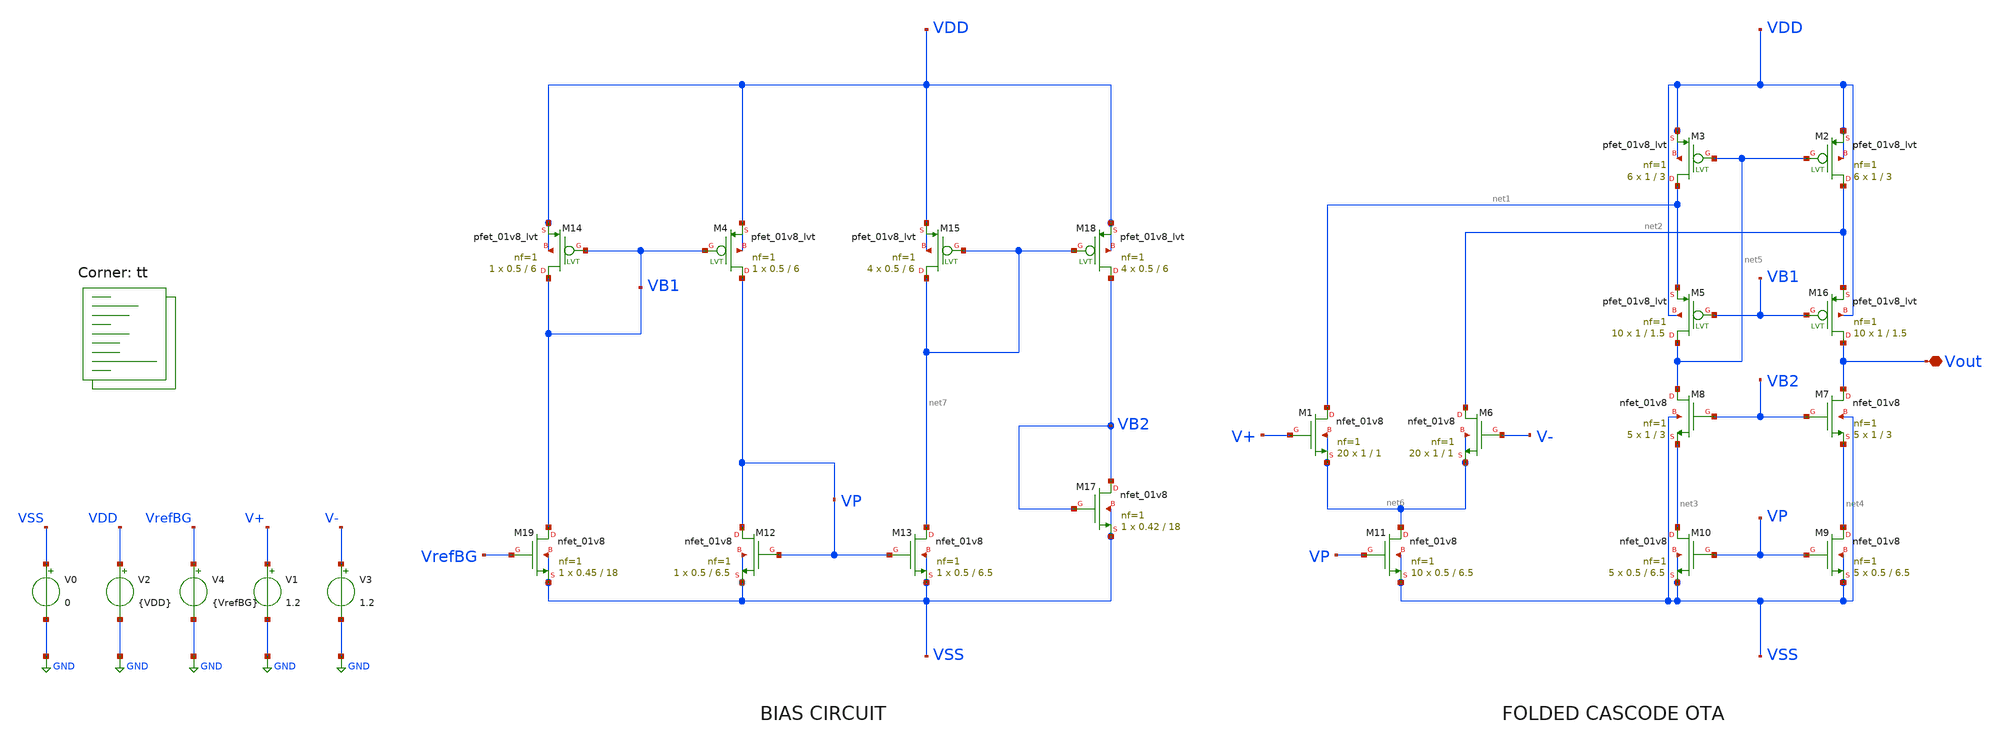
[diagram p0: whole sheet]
** sch_path: openfasoc/generators/curref-gen/sch/Folded_cascode_op.sch
**.subckt Folded_cascode_op Vout
*.iopin Vout
XM6 net2 V- net6 net6 sky130_fd_pr__nfet_01v8 L=1 W=1 nf=1 ad='int((nf+1)/2) * W/nf * 0.29' as='int((nf+2)/2) * W/nf * 0.29'
+ pd='2*int((nf+1)/2) * (W/nf + 0.29)' ps='2*int((nf+2)/2) * (W/nf + 0.29)' nrd='0.29 / W' nrs='0.29 / W'
+ sa=0 sb=0 sd=0 mult=20 m=20
XM7 Vout VB2 net4 VSS sky130_fd_pr__nfet_01v8 L=3 W=1 nf=1 ad='int((nf+1)/2) * W/nf * 0.29' as='int((nf+2)/2) * W/nf * 0.29'
+ pd='2*int((nf+1)/2) * (W/nf + 0.29)' ps='2*int((nf+2)/2) * (W/nf + 0.29)' nrd='0.29 / W' nrs='0.29 / W'
+ sa=0 sb=0 sd=0 mult=5 m=5
XM8 net5 VB2 net3 VSS sky130_fd_pr__nfet_01v8 L=3 W=1 nf=1 ad='int((nf+1)/2) * W/nf * 0.29' as='int((nf+2)/2) * W/nf * 0.29'
+ pd='2*int((nf+1)/2) * (W/nf + 0.29)' ps='2*int((nf+2)/2) * (W/nf + 0.29)' nrd='0.29 / W' nrs='0.29 / W'
+ sa=0 sb=0 sd=0 mult=5 m=5
XM9 net4 VP VSS VSS sky130_fd_pr__nfet_01v8 L=6.5 W=0.5 nf=1 ad='int((nf+1)/2) * W/nf * 0.29' as='int((nf+2)/2) * W/nf * 0.29'
+ pd='2*int((nf+1)/2) * (W/nf + 0.29)' ps='2*int((nf+2)/2) * (W/nf + 0.29)' nrd='0.29 / W' nrs='0.29 / W'
+ sa=0 sb=0 sd=0 mult=5 m=5
XM10 net3 VP VSS VSS sky130_fd_pr__nfet_01v8 L=6.5 W=0.5 nf=1 ad='int((nf+1)/2) * W/nf * 0.29' as='int((nf+2)/2) * W/nf * 0.29'
+ pd='2*int((nf+1)/2) * (W/nf + 0.29)' ps='2*int((nf+2)/2) * (W/nf + 0.29)' nrd='0.29 / W' nrs='0.29 / W'
+ sa=0 sb=0 sd=0 mult=5 m=5
XM11 net6 VP VSS VSS sky130_fd_pr__nfet_01v8 L=6.5 W=0.5 nf=1 ad='int((nf+1)/2) * W/nf * 0.29' as='int((nf+2)/2) * W/nf * 0.29'
+ pd='2*int((nf+1)/2) * (W/nf + 0.29)' ps='2*int((nf+2)/2) * (W/nf + 0.29)' nrd='0.29 / W' nrs='0.29 / W'
+ sa=0 sb=0 sd=0 mult=10 m=10
XM1 net1 V+ net6 net6 sky130_fd_pr__nfet_01v8 L=1 W=1 nf=1 ad='int((nf+1)/2) * W/nf * 0.29' as='int((nf+2)/2) * W/nf * 0.29'
+ pd='2*int((nf+1)/2) * (W/nf + 0.29)' ps='2*int((nf+2)/2) * (W/nf + 0.29)' nrd='0.29 / W' nrs='0.29 / W'
+ sa=0 sb=0 sd=0 mult=20 m=20
XM12 VP VP VSS VSS sky130_fd_pr__nfet_01v8 L=6.5 W=0.5 nf=1 ad='int((nf+1)/2) * W/nf * 0.29' as='int((nf+2)/2) * W/nf * 0.29'
+ pd='2*int((nf+1)/2) * (W/nf + 0.29)' ps='2*int((nf+2)/2) * (W/nf + 0.29)' nrd='0.29 / W' nrs='0.29 / W'
+ sa=0 sb=0 sd=0 mult=1 m=1
XM13 net7 VP VSS VSS sky130_fd_pr__nfet_01v8 L=6.5 W=0.5 nf=1 ad='int((nf+1)/2) * W/nf * 0.29' as='int((nf+2)/2) * W/nf * 0.29'
+ pd='2*int((nf+1)/2) * (W/nf + 0.29)' ps='2*int((nf+2)/2) * (W/nf + 0.29)' nrd='0.29 / W' nrs='0.29 / W'
+ sa=0 sb=0 sd=0 mult=1 m=1
XM17 VB2 VB2 VSS VSS sky130_fd_pr__nfet_01v8 L=18 W=0.42 nf=1 ad='int((nf+1)/2) * W/nf * 0.29' as='int((nf+2)/2) * W/nf * 0.29'
+ pd='2*int((nf+1)/2) * (W/nf + 0.29)' ps='2*int((nf+2)/2) * (W/nf + 0.29)' nrd='0.29 / W' nrs='0.29 / W'
+ sa=0 sb=0 sd=0 mult=1 m=1
XM18 VB2 net7 VDD VDD sky130_fd_pr__pfet_01v8_lvt L=6 W=0.5 nf=1 ad='int((1 + 1)/2) * 0.5 / 1 * 0.29'
+ as='int((1 + 2)/2) * 0.5 / 1 * 0.29' pd='2*int((1 + 1)/2) * (0.5 / 1 + 0.29)' ps='2*int((1 + 2)/2) * (0.5 / 1 + 0.29)'
+ nrd='0.29 / 0.5 ' nrs='0.29 / 0.5 ' sa=0 sb=0 sd=0 mult=4 m=4
XM15 net7 net7 VDD VDD sky130_fd_pr__pfet_01v8_lvt L=6 W=0.5 nf=1 ad='int((1 + 1)/2) * 0.5 / 1 * 0.29'
+ as='int((1 + 2)/2) * 0.5 / 1 * 0.29' pd='2*int((1 + 1)/2) * (0.5 / 1 + 0.29)' ps='2*int((1 + 2)/2) * (0.5 / 1 + 0.29)'
+ nrd='0.29 / 0.5 ' nrs='0.29 / 0.5 ' sa=0 sb=0 sd=0 mult=4 m=4
XM3 net1 net5 VDD VDD sky130_fd_pr__pfet_01v8_lvt L=3 W=1 nf=1 ad='int((1 + 1)/2) * 1 / 1 * 0.29' as='int((1 + 2)/2) * 1 / 1 * 0.29'
+ pd='2*int((1 + 1)/2) * (1 / 1 + 0.29)' ps='2*int((1 + 2)/2) * (1 / 1 + 0.29)' nrd='0.29 / 1 ' nrs='0.29 / 1 '
+ sa=0 sb=0 sd=0 mult=6 m=6
XM2 net2 net5 VDD VDD sky130_fd_pr__pfet_01v8_lvt L=3 W=1 nf=1 ad='int((1 + 1)/2) * 1 / 1 * 0.29' as='int((1 + 2)/2) * 1 / 1 * 0.29'
+ pd='2*int((1 + 1)/2) * (1 / 1 + 0.29)' ps='2*int((1 + 2)/2) * (1 / 1 + 0.29)' nrd='0.29 / 1 ' nrs='0.29 / 1 '
+ sa=0 sb=0 sd=0 mult=6 m=6
XM5 net5 VB1 net1 VDD sky130_fd_pr__pfet_01v8_lvt L=1.5 W=1 nf=1 ad='int((1 + 1)/2) * 1 / 1 * 0.29' as='int((1 + 2)/2) * 1 / 1 * 0.29'
+ pd='2*int((1 + 1)/2) * (1 / 1 + 0.29)' ps='2*int((1 + 2)/2) * (1 / 1 + 0.29)' nrd='0.29 / 1 ' nrs='0.29 / 1 '
+ sa=0 sb=0 sd=0 mult=10 m=10
XM16 Vout VB1 net2 VDD sky130_fd_pr__pfet_01v8_lvt L=1.5 W=1 nf=1 ad='int((1 + 1)/2) * 1 / 1 * 0.29'
+ as='int((1 + 2)/2) * 1 / 1 * 0.29' pd='2*int((1 + 1)/2) * (1 / 1 + 0.29)' ps='2*int((1 + 2)/2) * (1 / 1 + 0.29)'
+ nrd='0.29 / 1 ' nrs='0.29 / 1 ' sa=0 sb=0 sd=0 mult=10 m=10
V0 VSS GND 0
V2 VDD GND {VDD}
V4 VrefBG GND {VrefBG}
V1 V+ GND 1.2
V3 V- GND 1.2
XM4 VP VB1 VDD VDD sky130_fd_pr__pfet_01v8_lvt L=6 W=0.5 nf=1 ad='int((1 + 1)/2) * 0.5 / 1 * 0.29' as='int((1 + 2)/2) * 0.5 / 1 * 0.29'
+ pd='2*int((1 + 1)/2) * (0.5 / 1 + 0.29)' ps='2*int((1 + 2)/2) * (0.5 / 1 + 0.29)' nrd='0.29 / 0.5 ' nrs='0.29 / 0.5 '
+ sa=0 sb=0 sd=0 mult=1 m=1
XM14 VB1 VB1 VDD VDD sky130_fd_pr__pfet_01v8_lvt L=6 W=0.5 nf=1 ad='int((1 + 1)/2) * 0.5 / 1 * 0.29'
+ as='int((1 + 2)/2) * 0.5 / 1 * 0.29' pd='2*int((1 + 1)/2) * (0.5 / 1 + 0.29)' ps='2*int((1 + 2)/2) * (0.5 / 1 + 0.29)'
+ nrd='0.29 / 0.5 ' nrs='0.29 / 0.5 ' sa=0 sb=0 sd=0 mult=1 m=1
XM19 VB1 VrefBG VSS VSS sky130_fd_pr__nfet_01v8 L=18 W=0.45 nf=1 ad='int((nf+1)/2) * W/nf * 0.29' as='int((nf+2)/2) * W/nf * 0.29'
+ pd='2*int((nf+1)/2) * (W/nf + 0.29)' ps='2*int((nf+2)/2) * (W/nf + 0.29)' nrd='0.29 / W' nrs='0.29 / W'
+ sa=0 sb=0 sd=0 mult=1 m=1
**** begin user architecture code
.lib $::SKYWATER_MODELS/sky130.lib.spice tt



.param VDD=1.8
.param VrefBG=1.2
.save  @m.xm1.msky130_fd_pr__nfet_01v8[gm]  v(@m.xm1.msky130_fd_pr__nfet_01v8[vth])  @m.xm1.msky130_fd_pr__nfet_01v8[gds]  @m.xm1.msky130_fd_pr__nfet_01v8[id]
  @m.xm6.msky130_fd_pr__nfet_01v8[gm]  v(@m.xm6.msky130_fd_pr__nfet_01v8[vth])
+  @m.xm6.msky130_fd_pr__nfet_01v8[gds]  @m.xm6.msky130_fd_pr__nfet_01v8[id]
  @m.xm7.msky130_fd_pr__nfet_01v8[gm]  v(@m.xm7.msky130_fd_pr__nfet_01v8[vth])
+  @m.xm7.msky130_fd_pr__nfet_01v8[gds]  @m.xm7.msky130_fd_pr__nfet_01v8[id]
  @m.xm8.msky130_fd_pr__nfet_01v8[gm]  v(@m.xm8.msky130_fd_pr__nfet_01v8[vth])
+  @m.xm8.msky130_fd_pr__nfet_01v8[gds]  @m.xm8.msky130_fd_pr__nfet_01v8[id]
  @m.xm9.msky130_fd_pr__nfet_01v8[gm]  v(@m.xm9.msky130_fd_pr__nfet_01v8[vth])
+  @m.xm9.msky130_fd_pr__nfet_01v8[gds]  @m.xm9.msky130_fd_pr__nfet_01v8[id]
  @m.xm10.msky130_fd_pr__nfet_01v8[gm]  v(@m.xm10.msky130_fd_pr__nfet_01v8[vth])
+  @m.xm10.msky130_fd_pr__nfet_01v8[gds]  @m.xm10.msky130_fd_pr__nfet_01v8[id]
  @m.xm11.msky130_fd_pr__nfet_01v8[gm]  v(@m.xm11.msky130_fd_pr__nfet_01v8[vth])
+  @m.xm11.msky130_fd_pr__nfet_01v8[gds]  @m.xm11.msky130_fd_pr__nfet_01v8[id]
  @m.xm12.msky130_fd_pr__nfet_01v8[gm]  v(@m.xm12.msky130_fd_pr__nfet_01v8[vth])
+  @m.xm12.msky130_fd_pr__nfet_01v8[gds]  @m.xm12.msky130_fd_pr__nfet_01v8[id]
  @m.xm13.msky130_fd_pr__nfet_01v8[gm]  v(@m.xm13.msky130_fd_pr__nfet_01v8[vth])
+  @m.xm13.msky130_fd_pr__nfet_01v8[gds]  @m.xm13.msky130_fd_pr__nfet_01v8[id]
  @m.xm17.msky130_fd_pr__nfet_01v8[gm]  v(@m.xm17.msky130_fd_pr__nfet_01v8[vth])
+  @m.xm17.msky130_fd_pr__nfet_01v8[gds]  @m.xm17.msky130_fd_pr__nfet_01v8[id]
  @m.xm19.msky130_fd_pr__nfet_01v8[gm]  v(@m.xm19.msky130_fd_pr__nfet_01v8[vth])
+  @m.xm19.msky130_fd_pr__nfet_01v8[gds]  @m.xm19.msky130_fd_pr__nfet_01v8[id]
  @m.xm2.msky130_fd_pr__pfet_01v8_lvt[gm]  v(@m.xm2.msky130_fd_pr__pfet_01v8_lvt[vth])
+  @m.xm2.msky130_fd_pr__pfet_01v8_lvt[gds]  @m.xm2.msky130_fd_pr__pfet_01v8_lvt[id]
  @m.xm3.msky130_fd_pr__pfet_01v8_lvt[gm]  v(@m.xm3.msky130_fd_pr__pfet_01v8_lvt[vth])
+  @m.xm3.msky130_fd_pr__pfet_01v8_lvt[gds]  @m.xm3.msky130_fd_pr__pfet_01v8_lvt[id]
  @m.xm4.msky130_fd_pr__pfet_01v8_lvt[gm]  v(@m.xm4.msky130_fd_pr__pfet_01v8_lvt[vth])
+  @m.xm4.msky130_fd_pr__pfet_01v8_lvt[gds]  @m.xm4.msky130_fd_pr__pfet_01v8_lvt[id]
  @m.xm5.msky130_fd_pr__pfet_01v8_lvt[gm]  v(@m.xm5.msky130_fd_pr__pfet_01v8_lvt[vth])
+  @m.xm5.msky130_fd_pr__pfet_01v8_lvt[gds]  @m.xm5.msky130_fd_pr__pfet_01v8_lvt[id]
  @m.xm14.msky130_fd_pr__pfet_01v8_lvt[gm]  v(@m.xm14.msky130_fd_pr__pfet_01v8_lvt[vth])
+  @m.xm14.msky130_fd_pr__pfet_01v8_lvt[gds]  @m.xm14.msky130_fd_pr__pfet_01v8_lvt[id]
  @m.xm15.msky130_fd_pr__pfet_01v8_lvt[gm]  v(@m.xm15.msky130_fd_pr__pfet_01v8_lvt[vth])
+  @m.xm15.msky130_fd_pr__pfet_01v8_lvt[gds]  @m.xm15.msky130_fd_pr__pfet_01v8_lvt[id]
  @m.xm16.msky130_fd_pr__pfet_01v8_lvt[gm]  v(@m.xm16.msky130_fd_pr__pfet_01v8_lvt[vth])
+  @m.xm16.msky130_fd_pr__pfet_01v8_lvt[gds]  @m.xm16.msky130_fd_pr__pfet_01v8_lvt[id]
  @m.xm18.msky130_fd_pr__pfet_01v8_lvt[gm]  v(@m.xm18.msky130_fd_pr__pfet_01v8_lvt[vth])
+  @m.xm18.msky130_fd_pr__pfet_01v8_lvt[gds]  @m.xm18.msky130_fd_pr__pfet_01v8_lvt[id]

.control
  save all
  op
  show
  write Folded_cascode_op.raw
.endc



**** end user architecture code
**.ends
.GLOBAL GND
.end
